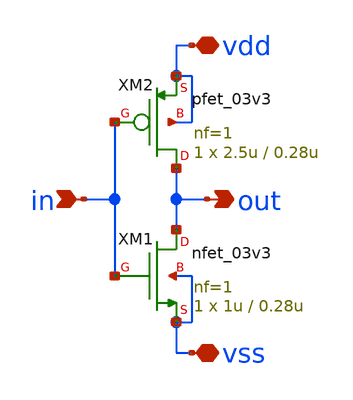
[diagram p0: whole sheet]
** sch_path: xschem/inverter.sch
**.subckt inverter in vdd vss out
*.ipin in
*.iopin vdd
*.iopin vss
*.opin out
XM1 out in vss vss nfet_03v3 L=0.28u W=1u nf=1 ad='int((nf+1)/2) * W/nf * 0.18u' as='int((nf+2)/2) * W/nf * 0.18u'
+ pd='2*int((nf+1)/2) * (W/nf + 0.18u)' ps='2*int((nf+2)/2) * (W/nf + 0.18u)' nrd='0.18u / W' nrs='0.18u / W'
+ sa=0 sb=0 sd=0 m=1
XM2 out in vdd vdd pfet_03v3 L=0.28u W=2.5u nf=1 ad='int((nf+1)/2) * W/nf * 0.18u' as='int((nf+2)/2) * W/nf * 0.18u'
+ pd='2*int((nf+1)/2) * (W/nf + 0.18u)' ps='2*int((nf+2)/2) * (W/nf + 0.18u)' nrd='0.18u / W' nrs='0.18u / W'
+ sa=0 sb=0 sd=0 m=1
**.ends
.end
